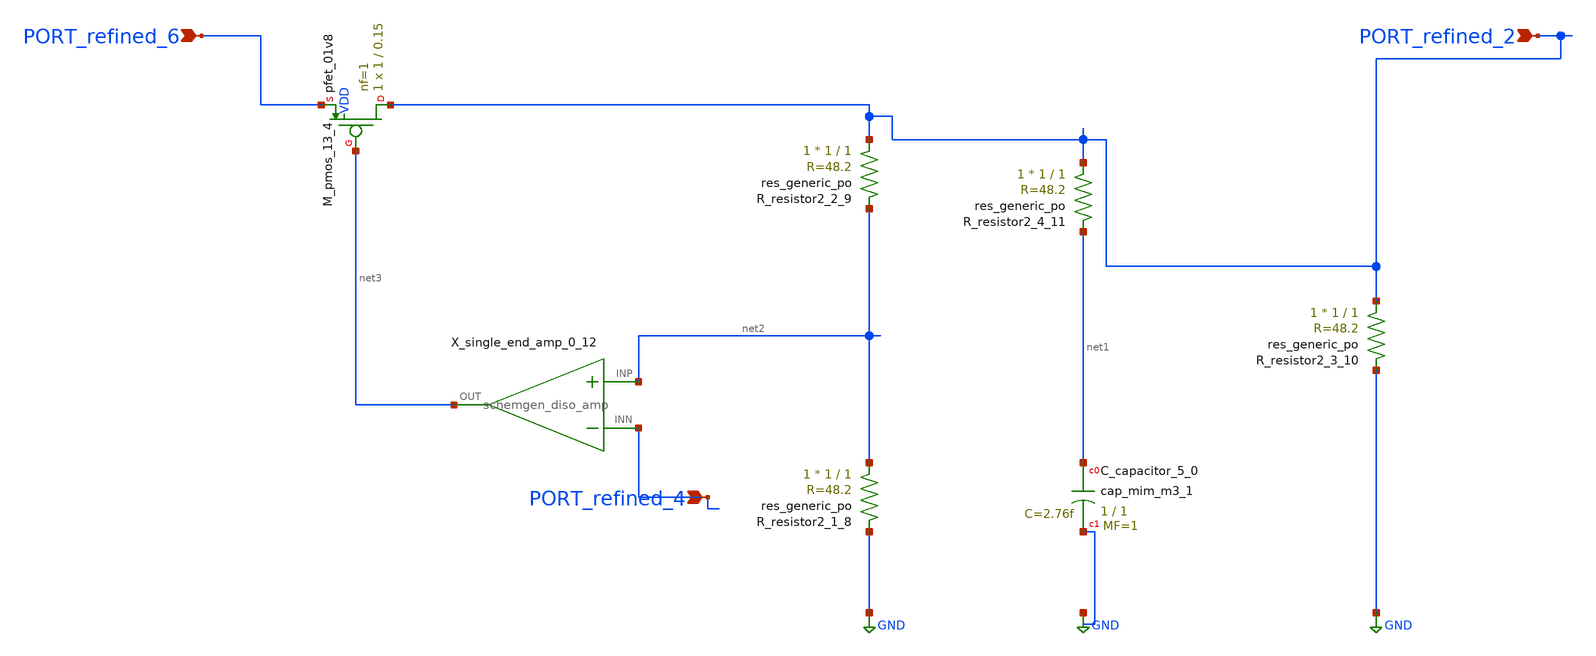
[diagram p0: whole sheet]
** sch_path: schematics/Image2Net/047.sch
**.subckt 047 PORT_refined_4 PORT_refined_6 PORT_refined_2
*.ipin PORT_refined_4
*.ipin PORT_refined_6
*.ipin PORT_refined_2
XC_capacitor_5_0 net1 GND sky130_fd_pr__cap_mim_m3_1 W=1 L=1 MF=1 m=1
XM_pmos_13_4 PORT_refined_2 net3 PORT_refined_6 VDD sky130_fd_pr__pfet_01v8 L=0.15 W=1 nf=1 ad='int((1 + 1)/2) * 1 / 1 * 0.29'
+ as='int((1 + 2)/2) * 1 / 1 * 0.29' pd='2*int((1 + 1)/2) * (1 / 1 + 0.29)' ps='2*int((1 + 2)/2) * (1 / 1 + 0.29)'
+ nrd='0.29 / 1 ' nrs='0.29 / 1 ' sa=0 sb=0 sd=0 mult=1 m=1
XR_resistor2_1_8 net2 GND sky130_fd_pr__res_generic_po W=1 L=1 m=1
XR_resistor2_2_9 PORT_refined_2 net2 sky130_fd_pr__res_generic_po W=1 L=1 m=1
XR_resistor2_3_10 PORT_refined_2 GND sky130_fd_pr__res_generic_po W=1 L=1 m=1
XR_resistor2_4_11 PORT_refined_2 net1 sky130_fd_pr__res_generic_po W=1 L=1 m=1
X_single_end_amp_0_12 net2 PORT_refined_4 net3 schemgen_diso_amp
**.ends

* expanding   symbol:  schemgen_diso_amp.sym # of pins=3
** sym_path: symbols/schemgen_diso_amp.sym
.subckt schemgen_diso_amp INP INN OUT
* SchemGen ideal op-amp: Vout = 1e5 * (V(INP) - V(INN))
E1 OUT 0 INP INN 1e5
.ends schemgen_diso_amp
.GLOBAL GND
.end
